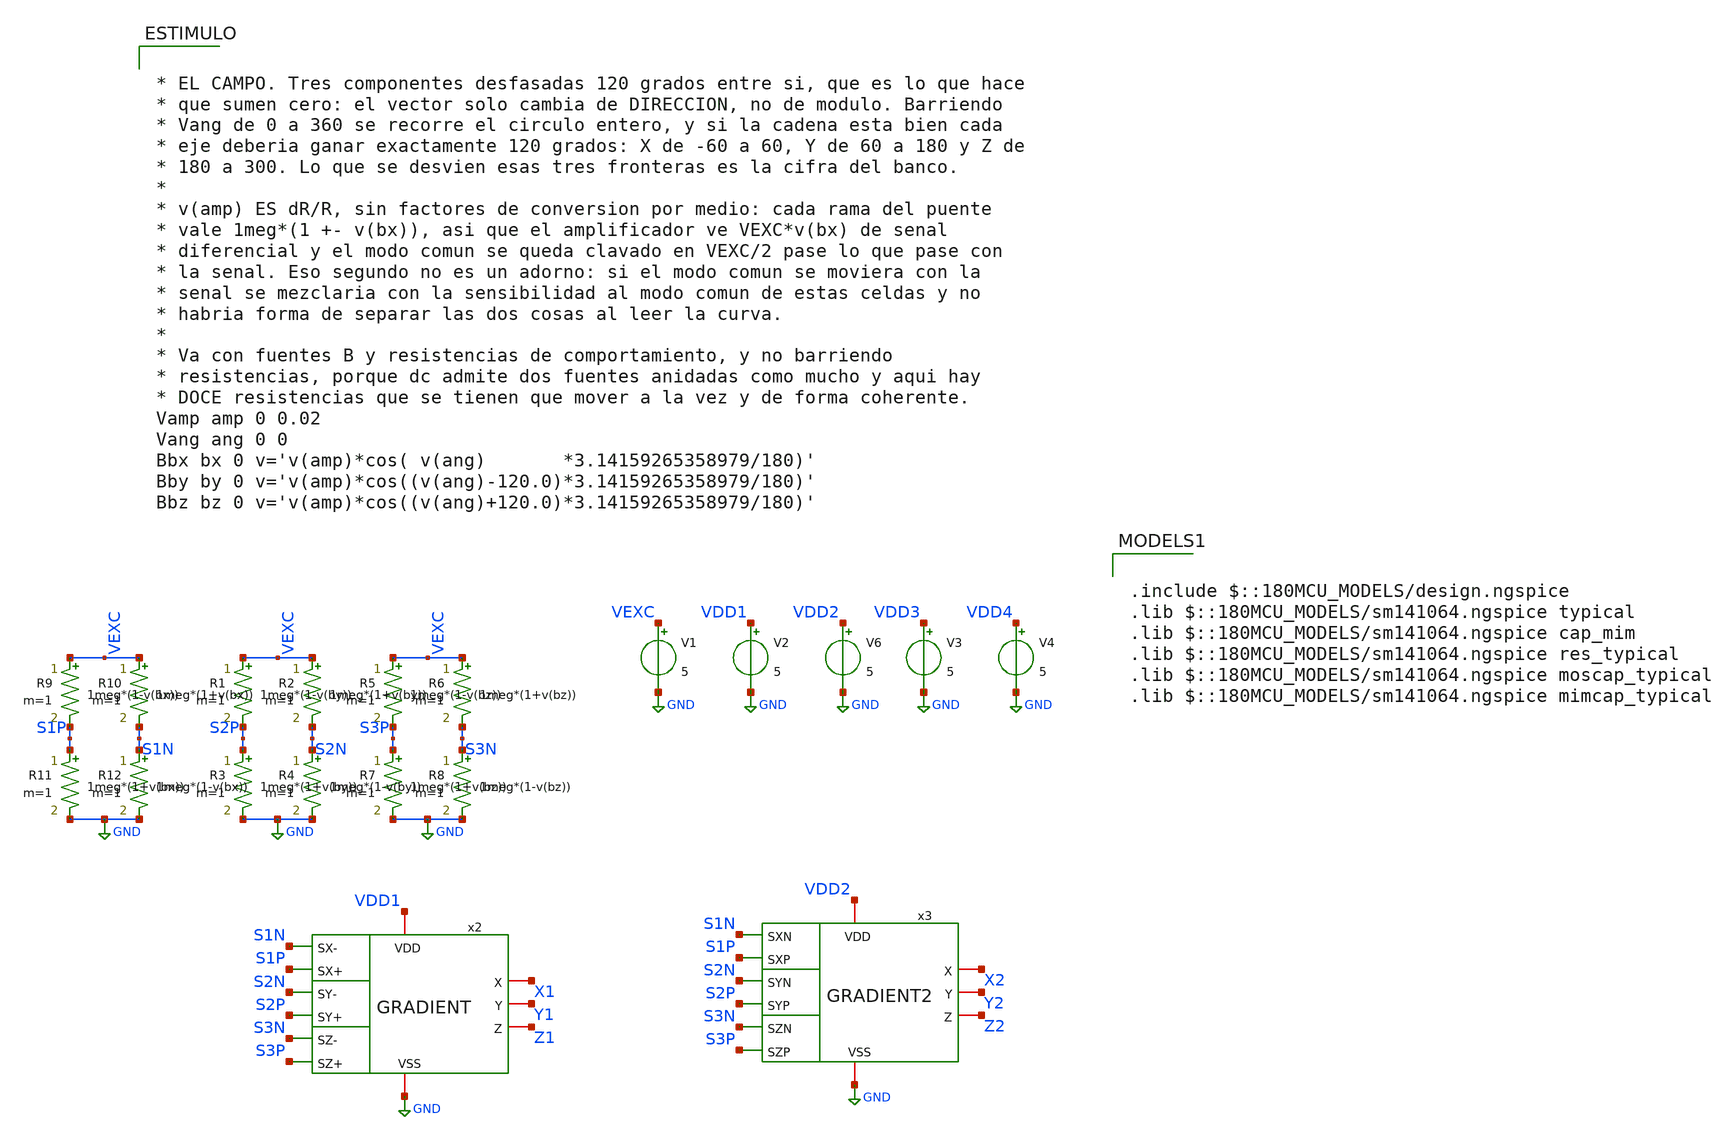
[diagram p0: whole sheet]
** sch_path: FINAL/XSCHEM/TEST_TOTAL/test_GRADIENT.sch
**.subckt test_GRADIENT
V1 VEXC GND 5
V2 VDD1 GND 5
V6 VDD2 GND 5
x2 S1N S1P VDD1 X1 S2N Y1 Z1 S2P GND S3N S3P GRADIENT
x3 S1N S1P VDD2 X2 S2N Y2 Z2 S2P GND S3N S3P GRADIENT2
R1 VEXC S2P r=' 1meg*(1-v(by)) '
R2 VEXC S2N r=' 1meg*(1+v(by)) '
R3 S2P GND r=' 1meg*(1+v(by)) '
R4 S2N GND r=' 1meg*(1-v(by)) '
V3 VDD3 GND 5
V4 VDD4 GND 5
R5 VEXC S3P r=' 1meg*(1-v(bz)) '
R6 VEXC S3N r=' 1meg*(1+v(bz)) '
R7 S3P GND r=' 1meg*(1+v(bz)) '
R8 S3N GND r=' 1meg*(1-v(bz)) '
R9 VEXC S1P r=' 1meg*(1-v(bx)) '
R10 VEXC S1N r=' 1meg*(1+v(bx)) '
R11 S1P GND r=' 1meg*(1+v(bx)) '
R12 S1N GND r=' 1meg*(1-v(bx)) '
**** begin user architecture code

.include $::180MCU_MODELS/design.ngspice
.lib $::180MCU_MODELS/sm141064.ngspice typical
.lib $::180MCU_MODELS/sm141064.ngspice cap_mim
.lib $::180MCU_MODELS/sm141064.ngspice res_typical
.lib $::180MCU_MODELS/sm141064.ngspice moscap_typical
.lib $::180MCU_MODELS/sm141064.ngspice mimcap_typical



* EL CAMPO. Tres componentes desfasadas 120 grados entre si, que es lo que hace
* que sumen cero: el vector solo cambia de DIRECCION, no de modulo. Barriendo
* Vang de 0 a 360 se recorre el circulo entero, y si la cadena esta bien cada
* eje deberia ganar exactamente 120 grados: X de -60 a 60, Y de 60 a 180 y Z de
* 180 a 300. Lo que se desvien esas tres fronteras es la cifra del banco.
*
* v(amp) ES dR/R, sin factores de conversion por medio: cada rama del puente
* vale 1meg*(1 +- v(bx)), asi que el amplificador ve VEXC*v(bx) de senal
* diferencial y el modo comun se queda clavado en VEXC/2 pase lo que pase con
* la senal. Eso segundo no es un adorno: si el modo comun se moviera con la
* senal se mezclaria con la sensibilidad al modo comun de estas celdas y no
* habria forma de separar las dos cosas al leer la curva.
*
* Va con fuentes B y resistencias de comportamiento, y no barriendo
* resistencias, porque dc admite dos fuentes anidadas como mucho y aqui hay
* DOCE resistencias que se tienen que mover a la vez y de forma coherente.
Vamp amp 0 0.02
Vang ang 0 0
Bbx bx 0 v='v(amp)*cos( v(ang)       *3.14159265358979/180)'
Bby by 0 v='v(amp)*cos((v(ang)-120.0)*3.14159265358979/180)'
Bbz bz 0 v='v(amp)*cos((v(ang)+120.0)*3.14159265358979/180)'




* LAS MISMAS DOS CADENAS, REHECHAS CON LOS BLOQUES EXTRAIDOS DEL LAYOUT v2.
* Cuelgan de los MISMOS seis nodos de sensor que las esquematicas y cada una
* lleva su propia alimentacion, para poder comparar tambien el consumo.
*
* La topologia es la de COMBINATION/GRADIENT.sch, copiada nodo a nodo:
*
*     amp X: S1N->INN  S1P->INP  -> SX        COMP XY: INN=SX INP=SY -> XY
*     amp Y: S2N->INN  S2P->INP  -> SY        COMP XZ: INN=SX INP=SZ -> XZ
*     amp Z: S3N->INN  S3P->INP  -> SZ        COMP YZ: INN=SY INP=SZ -> YZ
*                                             DECODER: XY XZ YZ -> X Y Z
*
* OJO CON EL ORDEN DE PUERTOS. xschem los emite en el orden de las lineas B del
* simbolo y magic en el orden en que los encuentra en el layout, y NO coinciden:
* el esquematico declara OPAM VDD INN OUT INP VSS y el extraido OPAM VSS VDD OUT
* INP INN. Cablear las dos igual significa cosas distintas y no da ningun error.
* Por eso encima de cada grupo va el orden de verdad, y por eso los ficheros son
* los _V2_ que produce TEST/preparar_extraidos.sh: renombra el subcircuito -- los
* dos declaran el mismo nombre y no se pueden incluir juntos -- y normaliza el
* orden. Fijate en que el OPAM_LIN_flat lleva OUT en medio y los otros no.
.include ../../../../layouts_v2/OPAM/mag/OPAM_V2_pex_rc.spice
.include ../../../../layouts_v2/OPAM_LIN_flat/mag/OPAM_LIN_flat_V2_pex_rc.spice
.include ../../../../layouts_v2/COMP/mag/COMP_V2_pex_rc.spice
.include ../../../../layouts_v2/DECODER/mag/DECODER_V2_pex_rc.spice

* --- G3: la cadena de G1, con el OPAM del layout v2
* .subckt OPAM_V2     VSS VDD OUT INP INN
XA31 GND VDD3 SX3 S1P S1N OPAM_V2
XA32 GND VDD3 SY3 S2P S2N OPAM_V2
XA33 GND VDD3 SZ3 S3P S3N OPAM_V2
* .subckt COMP_V2     VSS VDD OUT INP INN
XC31 GND VDD3 XY3 SY3 SX3 COMP_V2
XC32 GND VDD3 XZ3 SZ3 SX3 COMP_V2
XC33 GND VDD3 YZ3 SZ3 SY3 COMP_V2
* .subckt DECODER_V2  VSS VDD YZ Z XY XZ Y X
XD3  GND VDD3 YZ3 Z3 XY3 XZ3 Y3 X3 DECODER_V2

* --- G4: la cadena de G2, con el OPAM_LIN_flat del layout v2
* .subckt OPAM_LIN_flat_V2  VSS VDD INP OUT INN
XA41 GND VDD4 S1P SX4 S1N OPAM_LIN_flat_V2
XA42 GND VDD4 S2P SY4 S2N OPAM_LIN_flat_V2
XA43 GND VDD4 S3P SZ4 S3N OPAM_LIN_flat_V2
* .subckt COMP_V2     VSS VDD OUT INP INN
XC41 GND VDD4 XY4 SY4 SX4 COMP_V2
XC42 GND VDD4 XZ4 SZ4 SX4 COMP_V2
XC43 GND VDD4 YZ4 SZ4 SY4 COMP_V2
* .subckt DECODER_V2  VSS VDD YZ Z XY XZ Y X
XD4  GND VDD4 YZ4 Z4 XY4 XZ4 Y4 X4 DECODER_V2




* OJO: ni una llave en este texto. xschem las cuenta para saber donde acaba el
* bloque de atributos y una sola dentro de un comentario lo corta por la mitad,
* dejando el netlist con el 'blabla' de la plantilla y sin dar ningun error.
*
* Este banco NO necesita fuente de modo comun, al contrario que test_comp_* y
* test_opam_*: alli el par de entrada eran dos puertas sin camino de continua a
* masa, y aqui el propio puente se lo da.
*
* Las senales intermedias de las cadenas esquematicas se sacan por nombre
* jerarquico, v(x2.SX) y compania. En las rehechas a mano los nodos son de
* primer nivel y se llaman SX3, XY3 y asi.
.save all
.control
* Fondo de escala de una AMR tipica: dR/R = 2 %, o sea 100 mV diferenciales.
alter Vamp = 0.02
dc Vang 0 360 0.5
wrdata ancho.txt v(X1) v(Y1) v(Z1) v(X2) v(Y2) v(Z2) v(X3) v(Y3) v(Z3) v(X4) v(Y4) v(Z4) v(x2.SX)
+ v(x2.SY) v(x2.SZ) v(x3.SX) v(x3.SY) v(x3.SZ) v(SX3) v(SY3) v(SZ3) v(SX4) v(SY4) v(SZ4) v(x2.net1) v(x2.net2)
+ v(x2.net3) v(x3.net1) v(x3.net2) v(x3.net3) v(XY3) v(XZ3) v(YZ3) v(XY4) v(XZ4) v(YZ4) v(S1P) v(S1N) v(S2P)
+ v(S2N) v(S3P) v(S3N) v(VEXC)*i(V1) v(VDD1)*i(V2) v(VDD2)*i(V6) v(VDD3)*i(V3) v(VDD4)*i(V4)
* Ventana fina: dR/R = 50 ppm, o sea 250 uV diferenciales.
alter Vamp = 50u
dc Vang 0 360 0.5
wrdata fino.txt v(X1) v(Y1) v(Z1) v(X2) v(Y2) v(Z2) v(X3) v(Y3) v(Z3) v(X4) v(Y4) v(Z4) v(x2.SX)
+ v(x2.SY) v(x2.SZ) v(x3.SX) v(x3.SY) v(x3.SZ) v(SX3) v(SY3) v(SZ3) v(SX4) v(SY4) v(SZ4) v(x2.net1) v(x2.net2)
+ v(x2.net3) v(x3.net1) v(x3.net2) v(x3.net3) v(XY3) v(XZ3) v(YZ3) v(XY4) v(XZ4) v(YZ4) v(S1P) v(S1N) v(S2P)
+ v(S2N) v(S3P) v(S3N) v(VEXC)*i(V1) v(VDD1)*i(V2) v(VDD2)*i(V6) v(VDD3)*i(V3) v(VDD4)*i(V4)
.endc


**** end user architecture code
**.ends
.GLOBAL GND
.end
